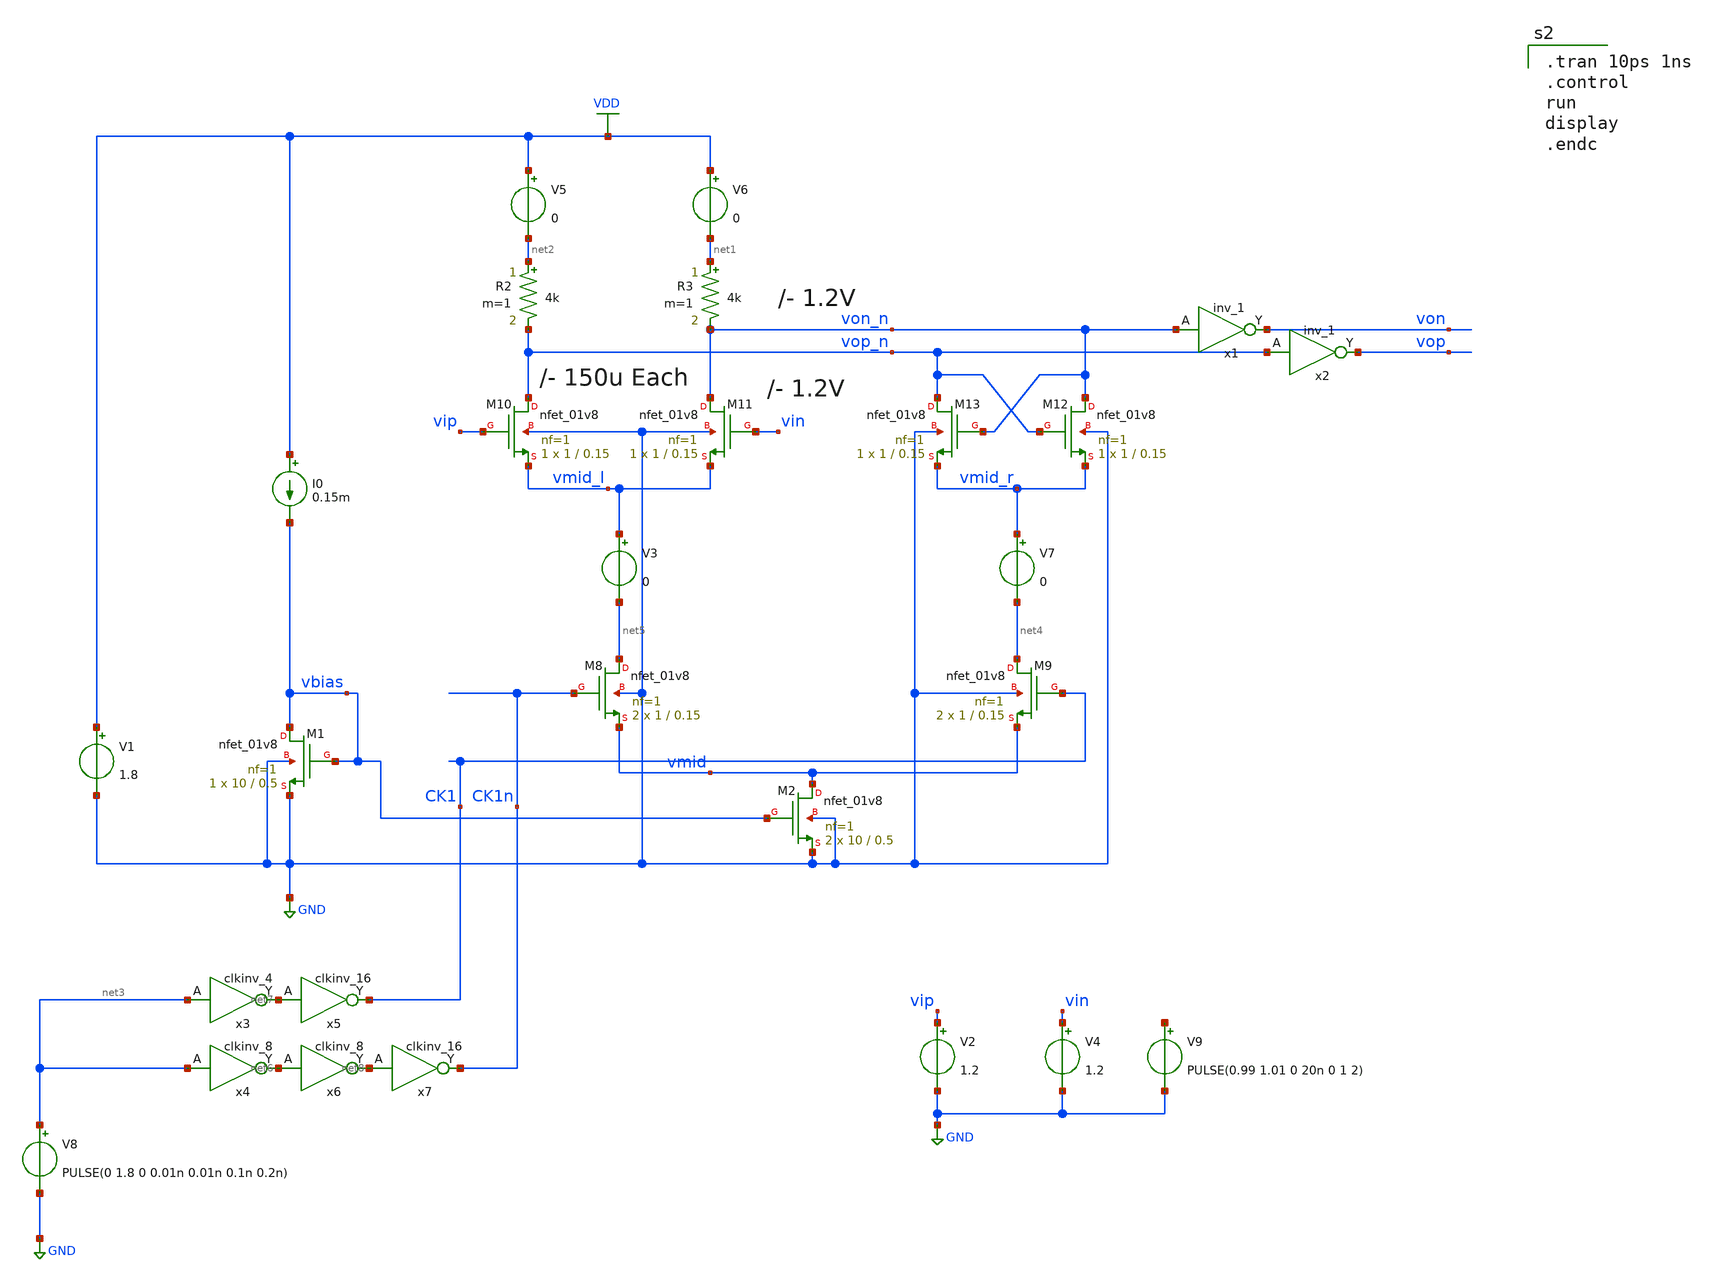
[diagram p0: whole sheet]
** sch_path: xschem/CML_latch_1.sch
**.subckt CML_latch_1
XM8 net5 CK1n vmid GND sky130_fd_pr__nfet_01v8 L=0.15 W=1 nf=1 ad='int((nf+1)/2) * W/nf * 0.29' as='int((nf+2)/2) * W/nf * 0.29'
+ pd='2*int((nf+1)/2) * (W/nf + 0.29)' ps='2*int((nf+2)/2) * (W/nf + 0.29)' nrd='0.29 / W' nrs='0.29 / W'
+ sa=0 sb=0 sd=0 mult=2 m=2
XM9 net4 CK1 vmid GND sky130_fd_pr__nfet_01v8 L=0.15 W=1 nf=1 ad='int((nf+1)/2) * W/nf * 0.29' as='int((nf+2)/2) * W/nf * 0.29'
+ pd='2*int((nf+1)/2) * (W/nf + 0.29)' ps='2*int((nf+2)/2) * (W/nf + 0.29)' nrd='0.29 / W' nrs='0.29 / W'
+ sa=0 sb=0 sd=0 mult=2 m=2
XM10 vop_n vip vmid_l GND sky130_fd_pr__nfet_01v8 L=0.15 W=1 nf=1 ad='int((nf+1)/2) * W/nf * 0.29' as='int((nf+2)/2) * W/nf * 0.29'
+ pd='2*int((nf+1)/2) * (W/nf + 0.29)' ps='2*int((nf+2)/2) * (W/nf + 0.29)' nrd='0.29 / W' nrs='0.29 / W'
+ sa=0 sb=0 sd=0 mult=1 m=1
XM11 von_n vin vmid_l GND sky130_fd_pr__nfet_01v8 L=0.15 W=1 nf=1 ad='int((nf+1)/2) * W/nf * 0.29' as='int((nf+2)/2) * W/nf * 0.29'
+ pd='2*int((nf+1)/2) * (W/nf + 0.29)' ps='2*int((nf+2)/2) * (W/nf + 0.29)' nrd='0.29 / W' nrs='0.29 / W'
+ sa=0 sb=0 sd=0 mult=1 m=1
XM12 von_n vop_n vmid_r GND sky130_fd_pr__nfet_01v8 L=0.15 W=1 nf=1 ad='int((nf+1)/2) * W/nf * 0.29'
+ as='int((nf+2)/2) * W/nf * 0.29' pd='2*int((nf+1)/2) * (W/nf + 0.29)' ps='2*int((nf+2)/2) * (W/nf + 0.29)'
+ nrd='0.29 / W' nrs='0.29 / W' sa=0 sb=0 sd=0 mult=1 m=1
XM13 vop_n von_n vmid_r GND sky130_fd_pr__nfet_01v8 L=0.15 W=1 nf=1 ad='int((nf+1)/2) * W/nf * 0.29'
+ as='int((nf+2)/2) * W/nf * 0.29' pd='2*int((nf+1)/2) * (W/nf + 0.29)' ps='2*int((nf+2)/2) * (W/nf + 0.29)'
+ nrd='0.29 / W' nrs='0.29 / W' sa=0 sb=0 sd=0 mult=1 m=1
R2 net2 vop_n 4k m=1
R3 net1 von_n 4k m=1
V5 VDD net2 0
V6 VDD net1 0
V8 net3 GND PULSE(0 1.8 0 0.01n 0.01n 0.1n 0.2n)
V1 VDD GND 1.8
XM1 vbias vbias GND GND sky130_fd_pr__nfet_01v8 L=0.5 W=10 nf=1 ad='int((nf+1)/2) * W/nf * 0.29' as='int((nf+2)/2) * W/nf * 0.29'
+ pd='2*int((nf+1)/2) * (W/nf + 0.29)' ps='2*int((nf+2)/2) * (W/nf + 0.29)' nrd='0.29 / W' nrs='0.29 / W'
+ sa=0 sb=0 sd=0 mult=1 m=1
x1 von_n gnd gnd vdd vdd von sky130_fd_sc_hs__inv_1
x2 vop_n gnd gnd vdd vdd vop sky130_fd_sc_hs__inv_1
V2 vip GND 1.2
V4 vin GND 1.2
XM2 vmid vbias GND GND sky130_fd_pr__nfet_01v8 L=0.5 W=10 nf=1 ad='int((nf+1)/2) * W/nf * 0.29' as='int((nf+2)/2) * W/nf * 0.29'
+ pd='2*int((nf+1)/2) * (W/nf + 0.29)' ps='2*int((nf+2)/2) * (W/nf + 0.29)' nrd='0.29 / W' nrs='0.29 / W'
+ sa=0 sb=0 sd=0 mult=2 m=2
I0 VDD vbias 0.15m
x4 net3 gnd gnd vdd vdd net6 sky130_fd_sc_hs__clkinv_8
x3 net3 gnd gnd vdd vdd net7 sky130_fd_sc_hs__clkinv_4
x5 net7 gnd gnd vdd vdd CK1 sky130_fd_sc_hs__clkinv_16
x6 net6 gnd gnd vdd vdd net8 sky130_fd_sc_hs__clkinv_8
x7 net8 gnd gnd vdd vdd CK1n sky130_fd_sc_hs__clkinv_16
V3 vmid_l net5 0
V7 vmid_r net4 0
V9 net9 GND PULSE(0.99 1.01 0 20n 0 1 2)
**** begin user architecture code

.tran 10ps 1ns
.control
run
display
.endc


.lib $::SKYWATER_MODELS/sky130.lib.spice tt
.include $::PDKPATH/libs.ref/sky130_fd_sc_hs/spice/sky130_fd_sc_hs.spice

**** end user architecture code
**.ends
.GLOBAL GND
.GLOBAL VDD
.end
